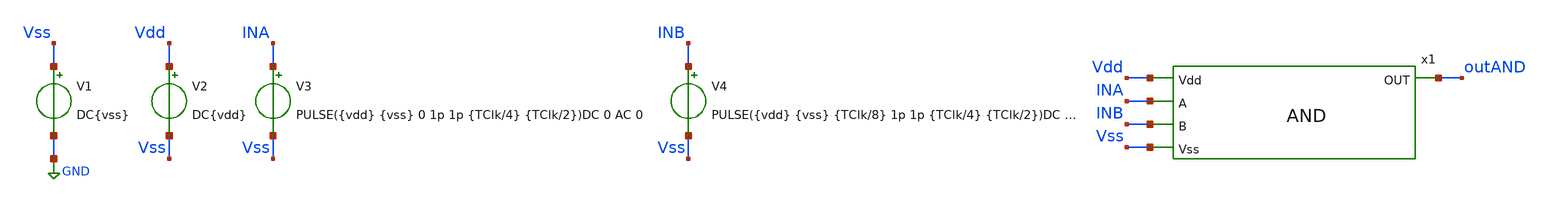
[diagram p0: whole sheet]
** sch_path: icdesign/sch/And/tb_AND.sch
**.subckt tb_AND
V1 Vss GND DC{vss}
V2 Vdd Vss DC{vdd}
V3 INA Vss PULSE({vdd} {vss} 0 1p 1p {TClk/4} {TClk/2})DC 0 AC 0
V4 INB Vss PULSE({vdd} {vss} {TClk/8} 1p 1p {TClk/4} {TClk/2})DC 0 AC 0
x1 Vdd INA INB outAND Vss AND
**** begin user architecture code





* Circuit Parameters
.param vdd  = 1.8
.param vss  = 0.0
.param Tclk = 10n
.options TEMP = 65.0


* Include Models
.lib ~/skywater/skywater-pdk/libraries/sky130_fd_pr_ngspice/latest/models/corners/sky130.lib TT


* OP Parameters & Singals to save
.save all


*Simulations
.control
  tran 0.01u 100n
  setplot tran1
  plot v(INA)v(INB)+2 v(outAND)+4
.endc
.end


**** end user architecture code
**.ends

* expanding   symbol:  And/AND.sym # of pins=5
** sym_path: icdesign/sch/And/AND.sym
** sch_path: icdesign/sch/And/AND.sch
.subckt AND Vdd A B OUT Vss
*.ipin Vss
*.ipin Vdd
*.ipin A
*.opin OUT
*.ipin B
XM1 net1 A Vdd Vdd sky130_fd_pr__pfet_01v8 L=0.15 W=0.75 nf=1 ad='int((nf+1)/2) * W/nf * 0.29' as='int((nf+2)/2) * W/nf * 0.29'
+ pd='2*int((nf+1)/2) * (W/nf + 0.29)' ps='2*int((nf+2)/2) * (W/nf + 0.29)' nrd='0.29 / W' nrs='0.29 / W'
+ sa=0 sb=0 sd=0 mult=2 m=2
XM2 net1 B Vdd Vdd sky130_fd_pr__pfet_01v8 L=0.15 W=0.75 nf=1 ad='int((nf+1)/2) * W/nf * 0.29' as='int((nf+2)/2) * W/nf * 0.29'
+ pd='2*int((nf+1)/2) * (W/nf + 0.29)' ps='2*int((nf+2)/2) * (W/nf + 0.29)' nrd='0.29 / W' nrs='0.29 / W'
+ sa=0 sb=0 sd=0 mult=2 m=2
XM5 OUT net1 Vdd Vdd sky130_fd_pr__pfet_01v8 L=0.15 W=0.75 nf=1 ad='int((nf+1)/2) * W/nf * 0.29' as='int((nf+2)/2) * W/nf * 0.29'
+ pd='2*int((nf+1)/2) * (W/nf + 0.29)' ps='2*int((nf+2)/2) * (W/nf + 0.29)' nrd='0.29 / W' nrs='0.29 / W'
+ sa=0 sb=0 sd=0 mult=2 m=2
XM6 OUT net1 Vss Vss sky130_fd_pr__nfet_01v8 L=0.15 W=0.75 nf=1 ad='int((nf+1)/2) * W/nf * 0.29' as='int((nf+2)/2) * W/nf * 0.29'
+ pd='2*int((nf+1)/2) * (W/nf + 0.29)' ps='2*int((nf+2)/2) * (W/nf + 0.29)' nrd='0.29 / W' nrs='0.29 / W'
+ sa=0 sb=0 sd=0 mult=1 m=1
XM3 net1 A net2 Vss sky130_fd_pr__nfet_01v8 L=0.15 W=0.75 nf=1 ad='int((nf+1)/2) * W/nf * 0.29' as='int((nf+2)/2) * W/nf * 0.29'
+ pd='2*int((nf+1)/2) * (W/nf + 0.29)' ps='2*int((nf+2)/2) * (W/nf + 0.29)' nrd='0.29 / W' nrs='0.29 / W'
+ sa=0 sb=0 sd=0 mult=2 m=2
XM4 net2 B Vss Vss sky130_fd_pr__nfet_01v8 L=0.15 W=0.75 nf=1 ad='int((nf+1)/2) * W/nf * 0.29' as='int((nf+2)/2) * W/nf * 0.29'
+ pd='2*int((nf+1)/2) * (W/nf + 0.29)' ps='2*int((nf+2)/2) * (W/nf + 0.29)' nrd='0.29 / W' nrs='0.29 / W'
+ sa=0 sb=0 sd=0 mult=2 m=2
.ends

.GLOBAL GND
.end
